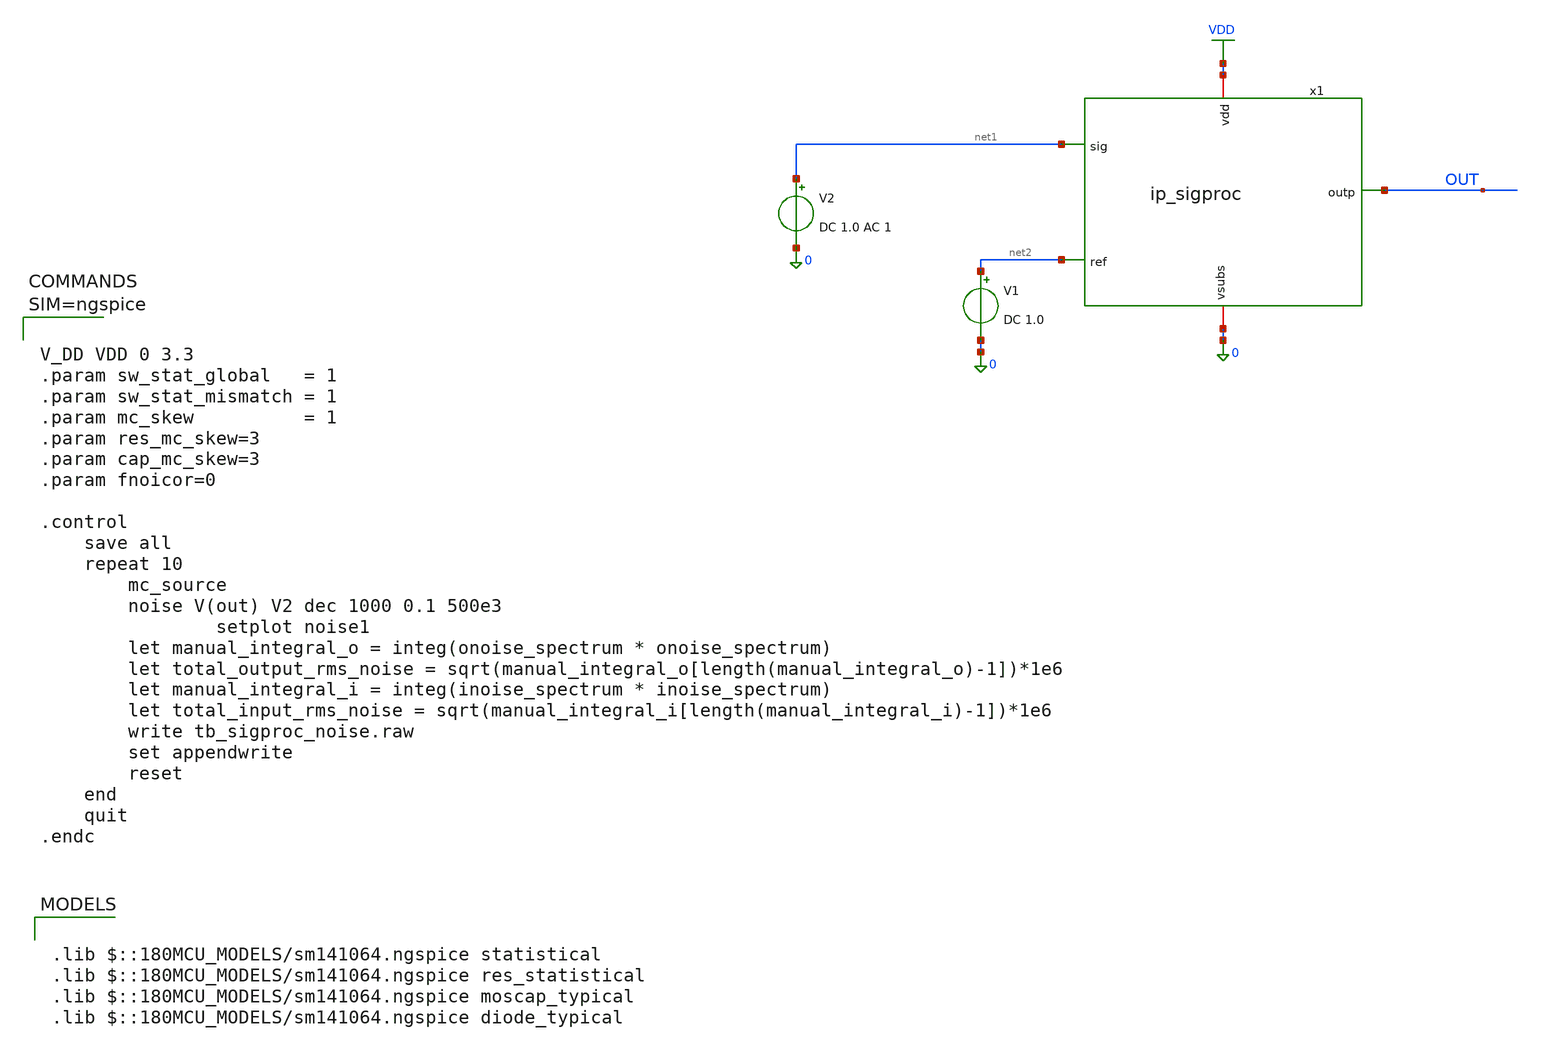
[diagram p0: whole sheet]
** sch_path: xschem/tb_sigproc_noise.sch
**.subckt tb_sigproc_noise
V2 net1 0 DC 1.0 AC 1
x1 VDD OUT net1 net2 0 ip_sigproc
V1 net2 0 DC 1.0
**** begin user architecture code

.lib $::180MCU_MODELS/sm141064.ngspice statistical
.lib $::180MCU_MODELS/sm141064.ngspice res_statistical
.lib $::180MCU_MODELS/sm141064.ngspice moscap_typical
.lib $::180MCU_MODELS/sm141064.ngspice diode_typical




V_DD VDD 0 3.3
.param sw_stat_global   = 1
.param sw_stat_mismatch = 1
.param mc_skew          = 1
.param res_mc_skew=3
.param cap_mc_skew=3
.param fnoicor=0

.control
	save all
	repeat 10
		mc_source
		noise V(out) V2 dec 1000 0.1 500e3
                setplot noise1
		let manual_integral_o = integ(onoise_spectrum * onoise_spectrum)
		let total_output_rms_noise = sqrt(manual_integral_o[length(manual_integral_o)-1])*1e6
		let manual_integral_i = integ(inoise_spectrum * inoise_spectrum)
		let total_input_rms_noise = sqrt(manual_integral_i[length(manual_integral_i)-1])*1e6
		write tb_sigproc_noise.raw
		set appendwrite
		reset
	end
	quit
.endc



**** end user architecture code
**.ends

* expanding   symbol:  ip_sigproc.sym # of pins=5
** sym_path: xschem/ip_sigproc.sym
** sch_path: xschem/ip_sigproc.sch
.subckt ip_sigproc vdd outp sig ref vsubs
*.ipin sig
*.ipin ref
*.iopin vdd
*.iopin vsubs
*.opin outp
x1 vdd net1 sig net1 vsubs ip_amplifier
x2 vdd outp ref net2 net6 ip_amplifier
XR1 net1 net2 net7 ppolyf_u_1k r_width=1e-6 r_length=10e-6 m=1
XR2 net2 net3 net8 ppolyf_u_1k r_width=1e-6 r_length=10e-6 m=1
XR3 net3 net4 net9 ppolyf_u_1k r_width=1e-6 r_length=10e-6 m=1
XR4 net4 net5 net10 ppolyf_u_1k r_width=1e-6 r_length=10e-6 m=1
XR5 net5 outp net11 ppolyf_u_1k r_width=1e-6 r_length=10e-6 m=1
XC1 outp net2 cap_pmos_03v3 c_width=12e-6 c_length=12e-6 m=1
XC2 net2 outp cap_pmos_03v3 c_width=12e-6 c_length=12e-6 m=1
.ends


* expanding   symbol:  xschem/ip_amplifier.sym # of pins=5
** sym_path: xschem/ip_amplifier.sym
** sch_path: xschem/ip_amplifier.sch
.subckt ip_amplifier VDD OUTP INP INN VSUBS
*.iopin VDD
*.iopin VSUBS
*.ipin INP
*.ipin INN
*.opin OUTP
XM1 COMP INP COMMON_ VDD pfet_03v3 L=5u W=18.0u nf=1 ad='int((nf+1)/2) * W/nf * 0.18u' as='int((nf+2)/2) * W/nf * 0.18u'
+ pd='2*int((nf+1)/2) * (W/nf + 0.18u)' ps='2*int((nf+2)/2) * (W/nf + 0.18u)' nrd='0.18u / W' nrs='0.18u / W'
+ sa=0 sb=0 sd=0 m=1 par=1
XM2 net6 INN COMMON_ VDD pfet_03v3 L=5u W=18.0u nf=1 ad='int((nf+1)/2) * W/nf * 0.18u' as='int((nf+2)/2) * W/nf * 0.18u'
+ pd='2*int((nf+1)/2) * (W/nf + 0.18u)' ps='2*int((nf+2)/2) * (W/nf + 0.18u)' nrd='0.18u / W' nrs='0.18u / W'
+ sa=0 sb=0 sd=0 m=1 par=1
XM3 net2 NBIAS VSUBS vsubs nfet_03v3 L=2u W=6u nf=1 ad='int((nf+1)/2) * W/nf * 0.18u' as='int((nf+2)/2) * W/nf * 0.18u'
+ pd='2*int((nf+1)/2) * (W/nf + 0.18u)' ps='2*int((nf+2)/2) * (W/nf + 0.18u)' nrd='0.18u / W' nrs='0.18u / W'
+ sa=0 sb=0 sd=0 m=2 par=2
XM4 net1 NBIAS VSUBS vsubs nfet_03v3 L=2u W=6u nf=1 ad='int((nf+1)/2) * W/nf * 0.18u' as='int((nf+2)/2) * W/nf * 0.18u'
+ pd='2*int((nf+1)/2) * (W/nf + 0.18u)' ps='2*int((nf+2)/2) * (W/nf + 0.18u)' nrd='0.18u / W' nrs='0.18u / W'
+ sa=0 sb=0 sd=0 m=1 par=1
XM7 NBIAS NBIAS net2 vsubs nfet_03v3 L=0.5u W=6u nf=1 ad='int((nf+1)/2) * W/nf * 0.18u' as='int((nf+2)/2) * W/nf * 0.18u'
+ pd='2*int((nf+1)/2) * (W/nf + 0.18u)' ps='2*int((nf+2)/2) * (W/nf + 0.18u)' nrd='0.18u / W' nrs='0.18u / W'
+ sa=0 sb=0 sd=0 m=4 par=4
XM8 net3 NBIAS net1 vsubs nfet_03v3 L=0.5u W=6u nf=1 ad='int((nf+1)/2) * W/nf * 0.18u' as='int((nf+2)/2) * W/nf * 0.18u'
+ pd='2*int((nf+1)/2) * (W/nf + 0.18u)' ps='2*int((nf+2)/2) * (W/nf + 0.18u)' nrd='0.18u / W' nrs='0.18u / W'
+ sa=0 sb=0 sd=0 m=4 par=4
XM9 net4 PBIAS VDD VDD pfet_03v3 L=2u W=6u nf=1 ad='int((nf+1)/2) * W/nf * 0.18u' as='int((nf+2)/2) * W/nf * 0.18u'
+ pd='2*int((nf+1)/2) * (W/nf + 0.18u)' ps='2*int((nf+2)/2) * (W/nf + 0.18u)' nrd='0.18u / W' nrs='0.18u / W'
+ sa=0 sb=0 sd=0 m=1 par=1
XM10 net5 PBIAS VDD VDD pfet_03v3 L=2u W=6u nf=1 ad='int((nf+1)/2) * W/nf * 0.18u' as='int((nf+2)/2) * W/nf * 0.18u'
+ pd='2*int((nf+1)/2) * (W/nf + 0.18u)' ps='2*int((nf+2)/2) * (W/nf + 0.18u)' nrd='0.18u / W' nrs='0.18u / W'
+ sa=0 sb=0 sd=0 m=1 par=1
XM11 PBIAS PBIAS net4 VDD pfet_03v3 L=0.5u W=6u nf=1 ad='int((nf+1)/2) * W/nf * 0.18u' as='int((nf+2)/2) * W/nf * 0.18u'
+ pd='2*int((nf+1)/2) * (W/nf + 0.18u)' ps='2*int((nf+2)/2) * (W/nf + 0.18u)' nrd='0.18u / W' nrs='0.18u / W'
+ sa=0 sb=0 sd=0 m=4 par=4
XM12 COMMON PBIAS net5 VDD pfet_03v3 L=0.5u W=6u nf=1 ad='int((nf+1)/2) * W/nf * 0.18u' as='int((nf+2)/2) * W/nf * 0.18u'
+ pd='2*int((nf+1)/2) * (W/nf + 0.18u)' ps='2*int((nf+2)/2) * (W/nf + 0.18u)' nrd='0.18u / W' nrs='0.18u / W'
+ sa=0 sb=0 sd=0 m=4 par=4
XM13 COMP net6 VSUBS vsubs nfet_03v3 L=5u W=6u nf=1 ad='int((nf+1)/2) * W/nf * 0.18u' as='int((nf+2)/2) * W/nf * 0.18u'
+ pd='2*int((nf+1)/2) * (W/nf + 0.18u)' ps='2*int((nf+2)/2) * (W/nf + 0.18u)' nrd='0.18u / W' nrs='0.18u / W'
+ sa=0 sb=0 sd=0 m=1 par=1
XM14 net6 net6 VSUBS vsubs nfet_03v3 L=5u W=6u nf=1 ad='int((nf+1)/2) * W/nf * 0.18u' as='int((nf+2)/2) * W/nf * 0.18u'
+ pd='2*int((nf+1)/2) * (W/nf + 0.18u)' ps='2*int((nf+2)/2) * (W/nf + 0.18u)' nrd='0.18u / W' nrs='0.18u / W'
+ sa=0 sb=0 sd=0 m=1 par=1
XM17 net8 PBIAS VDD VDD pfet_03v3 L=0.5u W=12u nf=1 ad='int((nf+1)/2) * W/nf * 0.18u' as='int((nf+2)/2) * W/nf * 0.18u'
+ pd='2*int((nf+1)/2) * (W/nf + 0.18u)' ps='2*int((nf+2)/2) * (W/nf + 0.18u)' nrd='0.18u / W' nrs='0.18u / W'
+ sa=0 sb=0 sd=0 m=2 par=2
XM18 OUTP COMP VSUBS vsubs nfet_03v3 L=0.5u W=12u nf=1 ad='int((nf+1)/2) * W/nf * 0.18u' as='int((nf+2)/2) * W/nf * 0.18u'
+ pd='2*int((nf+1)/2) * (W/nf + 0.18u)' ps='2*int((nf+2)/2) * (W/nf + 0.18u)' nrd='0.18u / W' nrs='0.18u / W'
+ sa=0 sb=0 sd=0 m=4 par=4
XR3 NBIAS net7 vsubs ppolyf_u_1k r_width=1e-6 r_length=48e-6 m=1
Vmeas VDD net7 0
Vmeas1 PBIAS net3 0
XC1 OUTP net9 cap_pmos_03v3 c_width=13.5e-6 c_length=18e-6 m=1
XC2 COMP net9 cap_pmos_03v3 c_width=13.5e-6 c_length=18e-6 m=1
Vmeas2 COMMON COMMON_ 0
Vmeas3 net8 OUTP 0
XR2 VDD net9 vsubs ppolyf_u_1k r_width=1e-6 r_length=96e-6 m=1
.ends

.GLOBAL VDD
.end
